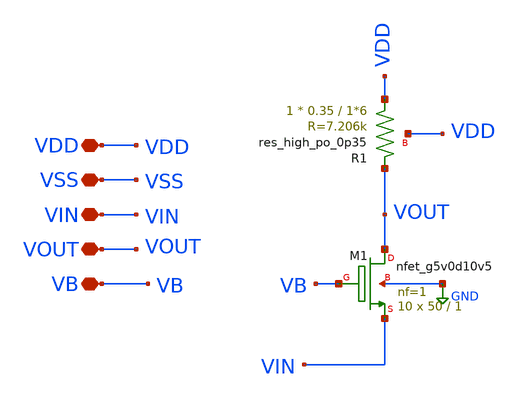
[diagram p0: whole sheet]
** sch_path: old stuff/amplifiers/single_stage_amps/basic_stages/cd_resistive_stage/cd_resistive_stage.sch
**.subckt cd_resistive_stage VDD VSS VIN VOUT VB
*.iopin VDD
*.iopin VSS
*.iopin VIN
*.iopin VOUT
*.iopin VB
XR1 VDD VOUT VDD sky130_fd_pr__res_high_po_0p35 L=1*6 mult=1 m=1
XM1 VOUT VB VIN GND sky130_fd_pr__nfet_g5v0d10v5 L=1 W=50 nf=1 ad='int((1 + 1)/2) * 50 / 1 * 0.29' as='int((1 + 2)/2) * 50 / 1 * 0.29'
+ pd='2*int((1 + 1)/2) * (50 / 1 + 0.29)' ps='2*int((1 + 2)/2) * (50 / 1 + 0.29)' nrd='0.29 / 50 ' nrs='0.29 / 50 '
+ sa=0 sb=0 sd=0 mult=10 m=10
**.ends
.GLOBAL GND
.end
